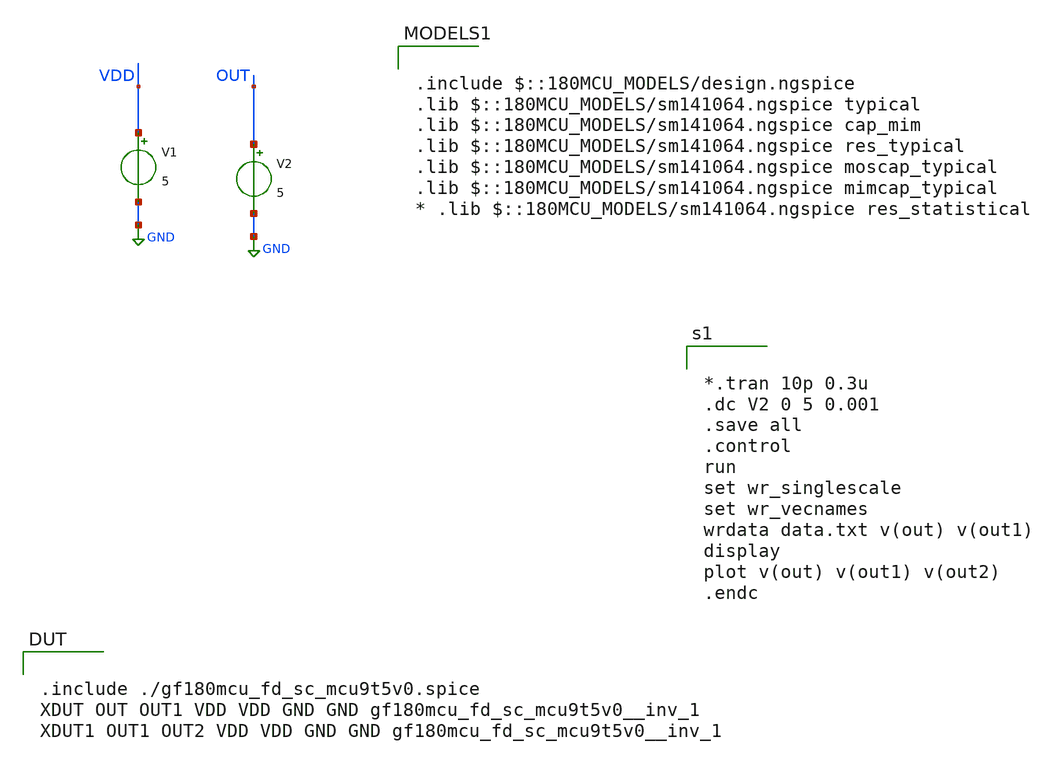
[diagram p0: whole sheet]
** sch_path: activities/opamp1Aysha/test2.sch
**.subckt test2
V1 VDD GND 5
V2 OUT GND 5
**** begin user architecture code


*.tran 10p 0.3u
.dc V2 0 5 0.001
.save all
.control
run
set wr_singlescale
set wr_vecnames
wrdata data.txt v(out) v(out1)
display
plot v(out) v(out1) v(out2)
.endc



.include $::180MCU_MODELS/design.ngspice
.lib $::180MCU_MODELS/sm141064.ngspice typical
.lib $::180MCU_MODELS/sm141064.ngspice cap_mim
.lib $::180MCU_MODELS/sm141064.ngspice res_typical
.lib $::180MCU_MODELS/sm141064.ngspice moscap_typical
.lib $::180MCU_MODELS/sm141064.ngspice mimcap_typical
* .lib $::180MCU_MODELS/sm141064.ngspice res_statistical


.include ./gf180mcu_fd_sc_mcu9t5v0.spice
XDUT OUT OUT1 VDD VDD GND GND gf180mcu_fd_sc_mcu9t5v0__inv_1
XDUT1 OUT1 OUT2 VDD VDD GND GND gf180mcu_fd_sc_mcu9t5v0__inv_1

**** end user architecture code
**.ends
.GLOBAL GND
.end
